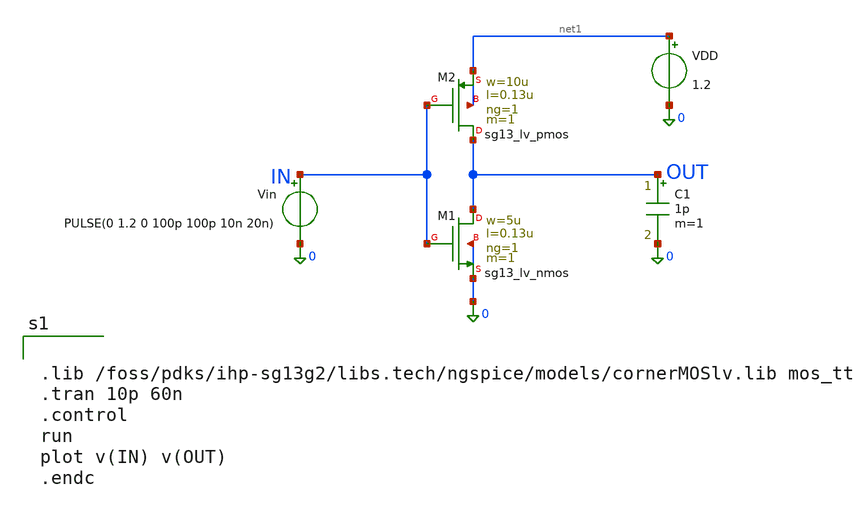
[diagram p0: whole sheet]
** sch_path: schematics/gate_driver.sch
**.subckt gate_driver
XM1 OUT IN 0 0 sg13_lv_nmos w=5u l=0.13u ng=1 m=1 mm_ok=1
Vin IN 0 PULSE(0 1.2 0 100p 100p 10n 20n)
VDD net1 0 1.2
XM2 OUT IN net1 net1 sg13_lv_pmos w=10u l=0.13u ng=1 m=1 mm_ok=1
C1 OUT 0 1p m=1
**** begin user architecture code


.lib /foss/pdks/ihp-sg13g2/libs.tech/ngspice/models/cornerMOSlv.lib mos_tt
.tran 10p 60n
.control
run
plot v(IN) v(OUT)
.endc


**** end user architecture code
**.ends
.end
